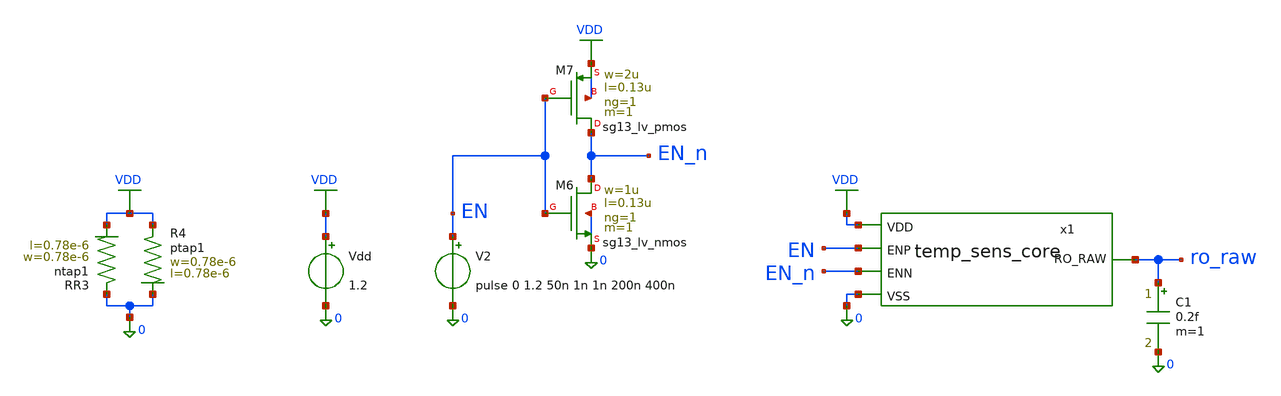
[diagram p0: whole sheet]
** sch_path: TSENSE8490-main/schematic/xschem/analog/temp-sens-core/testbenches/temp-sens-core_temp-sweep-tb.sch
**.subckt temp-sens-core_temp-sweep-tb
Vdd VDD 0 1.2
XR3 0 VDD ntap1 R=262.8 w=0.78e-6 l=0.78e-6
XR4 VDD 0 ptap1 R=262.8 w=0.78e-6 l=0.78e-6
x1 EN EN_n ro_raw VDD 0 temp_sens_core
XM6 EN_n EN 0 0 sg13_lv_nmos w=1u l=0.13u ng=1 m=1 mm_ok=1
XM7 EN_n EN VDD VDD sg13_lv_pmos w=2u l=0.13u ng=1 m=1 mm_ok=1
V2 EN 0 pulse 0 1.2 50n 1n 1n 200n 400n
C1 ro_raw 0 0.2f m=1
**** begin user architecture code



** ngr_lib cornerMOSlv.lib mos_tt mos_ff mos_ss mos_tt_mismatch
** ngr_lib cornerRES.lib res_typ
** ngr_out f
** ngr_name temp-sens-core_temp-sweep-tb

.option rshunt=1e12
.option klu
*.param cpar=0
*.param lstarv=0.18u
.control
let temp_start = -20
let temp_stop = 140
let temp_delta = 10

* Create one plot that will hold the sweep results
setplot new
set scratch = $curplot

compose temperature start=$&temp_start stop=$&temp_stop step=$&temp_delta
let frequency = vector(length(temperature))

let i = 0
let tcur = temp_start
while tcur <= temp_stop
  option temp = $&tcur

  tran 0.05n 300n

  meas tran tperiod
  + TRIG v(ro_raw) VAL=0.6 RISE=2 TD=75n
  + TARG v(ro_raw) VAL=0.6 RISE=3 TD=75n

  * Remember the just-created tran plot
  set dt = $curplot

  * Go back to the scratch plot before touching loop variables
  setplot $scratch

  if tcur = 20
    write temp-sens-core_temp-sweep_temp25_wave.raw {$dt}.time {$dt}.v(ro_raw) {$dt}.en {$dt}.en_n
    let time25 = {$dt}.time
    let f = 1/{$dt}.tperiod
    print f
    let ro_raw25 = {$dt}.v(ro_raw)
  end

  let frequency[i] = 1/{$dt}.tperiod
  let tcur = tcur + temp_delta
  let i = i+1
end

setplot $scratch

*settype temp-sweep temperature
settype frequency frequency
*setscale frequency temperature
**write temp-sens-core_temp-sweep.raw temperature frequency
write $rawfile temperature ro_raw en en_n frequency
.endc






.lib cornerMOSlv.lib mos_tt
.lib cornerMOShv.lib mos_tt
.lib cornerRES.lib res_typ
.lib cornerDIO.lib dio_tt






.include sg13cmos5l_stdcell.spice



**** end user architecture code
**.ends

* expanding   symbol:  analog/temp-sens-core/temp_sens_core.sym # of pins=5
** sym_path: TSENSE8490-main/schematic/xschem/lvs-view/analog/temp-sens-core/temp_sens_core.sym
** sch_path: TSENSE8490-main/schematic/xschem/lvs-view/analog/temp-sens-core/temp_sens_core.sch
.subckt temp_sens_core ENP ENN RO_RAW VDD VSS
*.opin RO_RAW
*.iopin VDD
*.iopin VSS
*.ipin ENP
*.ipin ENN
XM1 net11 vgp VDD VDD sg13_lv_pmos w=1.5u l={lstarv} ng=1 m=1 mm_ok=1
XM21 vgp ENP VDD VDD sg13_lv_pmos w=10u l=0.13u ng=1 m=1 mm_ok=1
XM22 vgn ENN VSS VSS sg13_lv_nmos w=10u l=0.13u ng=1 m=1 mm_ok=1
XM23 vgp vgp VDD VDD sg13_lv_pmos w=1.5u l={lstarv} ng=1 m=1 mm_ok=1
XM24 vgn vgn VSS VSS sg13_lv_nmos w=1.5u l={lstarv} ng=1 m=1 mm_ok=1
XM4 net20 vgn VSS VSS sg13_lv_nmos w=1.5u l={lstarv} ng=1 m=1 mm_ok=1
XM5 net12 vgp VDD VDD sg13_lv_pmos w=1.5u l={lstarv} ng=1 m=1 mm_ok=1
XM8 net21 vgn VSS VSS sg13_lv_nmos w=1.5u l={lstarv} ng=1 m=1 mm_ok=1
XM9 net13 vgp VDD VDD sg13_lv_pmos w=1.5u l={lstarv} ng=1 m=1 mm_ok=1
XM12 net22 vgn VSS VSS sg13_lv_nmos w=1.5u l={lstarv} ng=1 m=1 mm_ok=1
XM13 net14 vgp VDD VDD sg13_lv_pmos w=1.5u l={lstarv} ng=1 m=1 mm_ok=1
XM16 net23 vgn VSS VSS sg13_lv_nmos w=1.5u l={lstarv} ng=1 m=1 mm_ok=1
XM17 net15 vgp VDD VDD sg13_lv_pmos w=1.5u l={lstarv} ng=1 m=1 mm_ok=1
XM20 net24 vgn VSS VSS sg13_lv_nmos w=1.5u l={lstarv} ng=1 m=1 mm_ok=1
XM25 net16 vgp VDD VDD sg13_lv_pmos w=1.5u l={lstarv} ng=1 m=1 mm_ok=1
XM28 net25 vgn VSS VSS sg13_lv_nmos w=1.5u l={lstarv} ng=1 m=1 mm_ok=1
XM29 net17 vgp VDD VDD sg13_lv_pmos w=1.5u l={lstarv} ng=1 m=1 mm_ok=1
XM32 net26 vgn VSS VSS sg13_lv_nmos w=1.5u l={lstarv} ng=1 m=1 mm_ok=1
XM2 VSS net1 vgp VDD sg13_lv_pmos w=1u l=0.13u ng=1 m=1 mm_ok=1
XM3 VDD net2 vgn VSS sg13_lv_nmos w=1u l=0.13u ng=1 m=1 mm_ok=1
XR6 VDD net1 sub! rsil w=0.5e-6 l=75e-6 m=1 mm_ok=1
XR7 net1 VSS sub! rsil w=0.5e-6 l=10e-6 m=1 mm_ok=1
XR1 net2 VSS sub! rsil w=0.5e-6 l=75e-6 m=1 mm_ok=1
XR2 VDD net2 sub! rsil w=0.5e-6 l=10e-6 m=1 mm_ok=1
XM6 net18 vgp VDD VDD sg13_lv_pmos w=1.5u l={lstarv} ng=1 m=1 mm_ok=1
XM7 net27 vgn VSS VSS sg13_lv_nmos w=1.5u l={lstarv} ng=1 m=1 mm_ok=1
XM10 net19 vgp VDD VDD sg13_lv_pmos w=1.5u l={lstarv} ng=1 m=1 mm_ok=1
XM11 net28 vgn VSS VSS sg13_lv_nmos w=1.5u l={lstarv} ng=1 m=1 mm_ok=1
XM14 RO_RAW ENP VDD VDD sg13_lv_pmos w=0.3u l=0.13u ng=1 m=1 mm_ok=1
XM15 net3 RO_RAW net20 VSS sg13_lv_nmos w=0.74u l=0.13u ng=1 m=1 mm_ok=1
XM18 net11 RO_RAW net3 VDD sg13_lv_pmos w=1.12u l=0.13u ng=1 m=1 mm_ok=1
XM19 net4 net3 net21 VSS sg13_lv_nmos w=0.74u l=0.13u ng=1 m=1 mm_ok=1
XM26 net12 net3 net4 VDD sg13_lv_pmos w=1.12u l=0.13u ng=1 m=1 mm_ok=1
XM27 net5 net4 net22 VSS sg13_lv_nmos w=0.74u l=0.13u ng=1 m=1 mm_ok=1
XM30 net13 net4 net5 VDD sg13_lv_pmos w=1.12u l=0.13u ng=1 m=1 mm_ok=1
XM31 net6 net5 net23 VSS sg13_lv_nmos w=0.74u l=0.13u ng=1 m=1 mm_ok=1
XM33 net14 net5 net6 VDD sg13_lv_pmos w=1.12u l=0.13u ng=1 m=1 mm_ok=1
XM34 net7 net6 net24 VSS sg13_lv_nmos w=0.74u l=0.13u ng=1 m=1 mm_ok=1
XM35 net15 net6 net7 VDD sg13_lv_pmos w=1.12u l=0.13u ng=1 m=1 mm_ok=1
XM36 net8 net7 net25 VSS sg13_lv_nmos w=0.74u l=0.13u ng=1 m=1 mm_ok=1
XM37 net16 net7 net8 VDD sg13_lv_pmos w=1.12u l=0.13u ng=1 m=1 mm_ok=1
XM38 net9 net8 net26 VSS sg13_lv_nmos w=0.74u l=0.13u ng=1 m=1 mm_ok=1
XM39 net17 net8 net9 VDD sg13_lv_pmos w=1.12u l=0.13u ng=1 m=1 mm_ok=1
XM40 net10 net9 net27 VSS sg13_lv_nmos w=0.74u l=0.13u ng=1 m=1 mm_ok=1
XM41 net18 net9 net10 VDD sg13_lv_pmos w=1.12u l=0.13u ng=1 m=1 mm_ok=1
XM42 RO_RAW net10 net28 VSS sg13_lv_nmos w=0.74u l=0.13u ng=1 m=1 mm_ok=1
XM43 net19 net10 RO_RAW VDD sg13_lv_pmos w=1.12u l=0.13u ng=1 m=1 mm_ok=1
.ends

.GLOBAL VDD
.end
